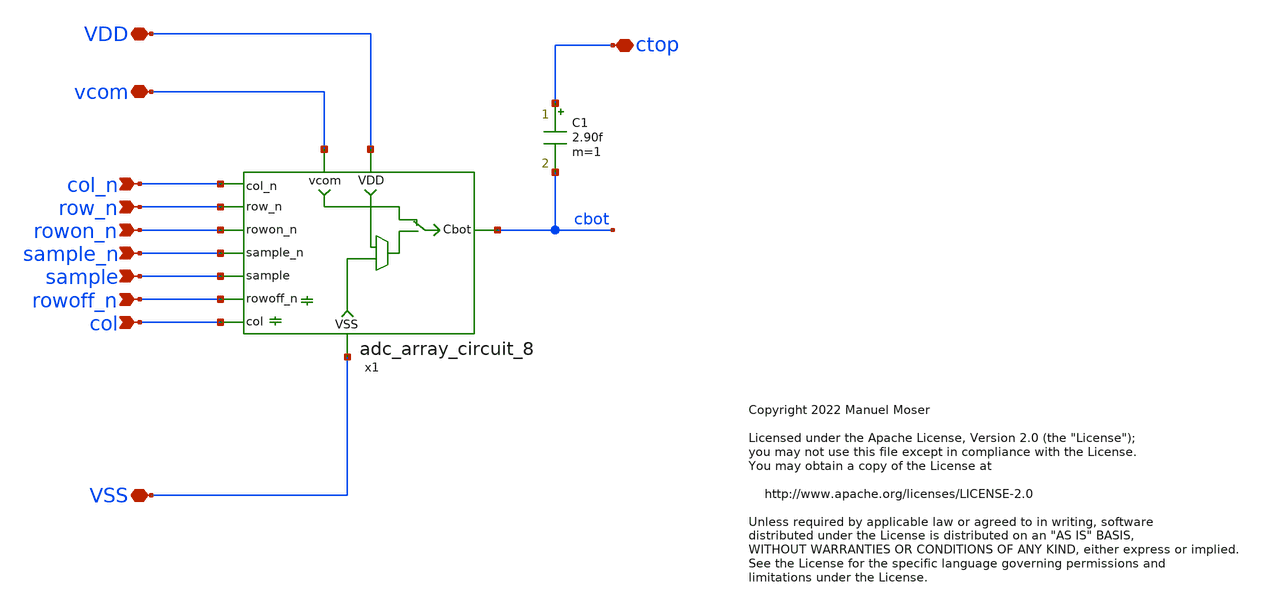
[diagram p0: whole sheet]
** sch_path: xschem/adc_array_wafflecap_8_8.sch
* Copyright 2022 Manuel Moser
* Licensed under the Apache License, Version 2.0 (the "License");
**.subckt adc_array_wafflecap_8_8 vcom VDD ctop VSS row_n col_n rowon_n sample_n sample rowoff_n col
*.iopin vcom
*.iopin VDD
*.iopin ctop
*.iopin VSS
*.ipin row_n
*.ipin col_n
*.ipin rowon_n
*.ipin sample_n
*.ipin sample
*.ipin rowoff_n
*.ipin col
C1 ctop cbot 2.90f m=1
x1 VDD col_n cbot row_n rowon_n sample_n vcom sample VSS rowoff_n col adc_array_circuit_8
**.ends

* expanding   symbol:  adc_array_circuit_8.sym # of pins=11
** sym_path: xschem/adc_array_circuit_8.sym
** sch_path: xschem/adc_array_circuit_8.sch
.subckt adc_array_circuit_8 VDD col_n Cbot row_n rowon_n sample_n vcom sample VSS rowoff_n col
*.ipin sample_n
*.ipin sample
*.iopin vcom
*.ipin col_n
*.ipin row_n
*.ipin rowon_n
*.iopin VDD
*.iopin VSS
*.iopin Cbot
*.ipin col
*.ipin rowoff_n
XM1 vcom sample Cbot VSS sky130_fd_pr__nfet_01v8 L=0.15 W=0.42 nf=1 ad='int((nf+1)/2) * W/nf * 0.29'
+ as='int((nf+2)/2) * W/nf * 0.29' pd='2*int((nf+1)/2) * (W/nf + 0.29)' ps='2*int((nf+2)/2) * (W/nf + 0.29)'
+ nrd='0.29 / W' nrs='0.29 / W' sa=0 sb=0 sd=0 mult=1 m=1
XM3 vcom sample_n Cbot VDD sky130_fd_pr__pfet_01v8 L=0.15 W=0.8 nf=1 ad='int((nf+1)/2) * W/nf * 0.29'
+ as='int((nf+2)/2) * W/nf * 0.29' pd='2*int((nf+1)/2) * (W/nf + 0.29)' ps='2*int((nf+2)/2) * (W/nf + 0.29)'
+ nrd='0.29 / W' nrs='0.29 / W' sa=0 sb=0 sd=0 mult=1 m=1
XM2 vdrv sample_n Cbot VSS sky130_fd_pr__nfet_01v8 L=0.15 W=0.42 nf=1 ad='int((nf+1)/2) * W/nf * 0.29'
+ as='int((nf+2)/2) * W/nf * 0.29' pd='2*int((nf+1)/2) * (W/nf + 0.29)' ps='2*int((nf+2)/2) * (W/nf + 0.29)'
+ nrd='0.29 / W' nrs='0.29 / W' sa=0 sb=0 sd=0 mult=1 m=1
XM4 vdrv sample Cbot VDD sky130_fd_pr__pfet_01v8 L=0.15 W=0.8 nf=1 ad='int((nf+1)/2) * W/nf * 0.29' as='int((nf+2)/2) * W/nf * 0.29'
+ pd='2*int((nf+1)/2) * (W/nf + 0.29)' ps='2*int((nf+2)/2) * (W/nf + 0.29)' nrd='0.29 / W' nrs='0.29 / W'
+ sa=0 sb=0 sd=0 mult=1 m=1
XM5 vint1 row_n vdrv VDD sky130_fd_pr__pfet_01v8 L=0.15 W=0.8 nf=1 ad='int((nf+1)/2) * W/nf * 0.29' as='int((nf+2)/2) * W/nf * 0.29'
+ pd='2*int((nf+1)/2) * (W/nf + 0.29)' ps='2*int((nf+2)/2) * (W/nf + 0.29)' nrd='0.29 / W' nrs='0.29 / W'
+ sa=0 sb=0 sd=0 mult=1 m=1
XM6 VDD col_n vint1 VDD sky130_fd_pr__pfet_01v8 L=0.15 W=0.8 nf=1 ad='int((nf+1)/2) * W/nf * 0.29' as='int((nf+2)/2) * W/nf * 0.29'
+ pd='2*int((nf+1)/2) * (W/nf + 0.29)' ps='2*int((nf+2)/2) * (W/nf + 0.29)' nrd='0.29 / W' nrs='0.29 / W'
+ sa=0 sb=0 sd=0 mult=1 m=1
XM7 VDD rowon_n vdrv VDD sky130_fd_pr__pfet_01v8 L=0.15 W=0.8 nf=1 ad='int((nf+1)/2) * W/nf * 0.29' as='int((nf+2)/2) * W/nf * 0.29'
+ pd='2*int((nf+1)/2) * (W/nf + 0.29)' ps='2*int((nf+2)/2) * (W/nf + 0.29)' nrd='0.29 / W' nrs='0.29 / W'
+ sa=0 sb=0 sd=0 mult=1 m=1
XM8 vint2 rowon_n vdrv VSS sky130_fd_pr__nfet_01v8 L=0.15 W=0.42 nf=1 ad='int((nf+1)/2) * W/nf * 0.29'
+ as='int((nf+2)/2) * W/nf * 0.29' pd='2*int((nf+1)/2) * (W/nf + 0.29)' ps='2*int((nf+2)/2) * (W/nf + 0.29)'
+ nrd='0.29 / W' nrs='0.29 / W' sa=0 sb=0 sd=0 mult=1 m=1
XM9 VSS col_n vint2 VSS sky130_fd_pr__nfet_01v8 L=0.15 W=0.42 nf=1 ad='int((nf+1)/2) * W/nf * 0.29' as='int((nf+2)/2) * W/nf * 0.29'
+ pd='2*int((nf+1)/2) * (W/nf + 0.29)' ps='2*int((nf+2)/2) * (W/nf + 0.29)' nrd='0.29 / W' nrs='0.29 / W'
+ sa=0 sb=0 sd=0 mult=1 m=1
XM10 VSS row_n vint2 VSS sky130_fd_pr__nfet_01v8 L=0.15 W=0.42 nf=1 ad='int((nf+1)/2) * W/nf * 0.29'
+ as='int((nf+2)/2) * W/nf * 0.29' pd='2*int((nf+1)/2) * (W/nf + 0.29)' ps='2*int((nf+2)/2) * (W/nf + 0.29)'
+ nrd='0.29 / W' nrs='0.29 / W' sa=0 sb=0 sd=0 mult=1 m=1
* noconn col
* noconn rowoff_n
.ends

.end
